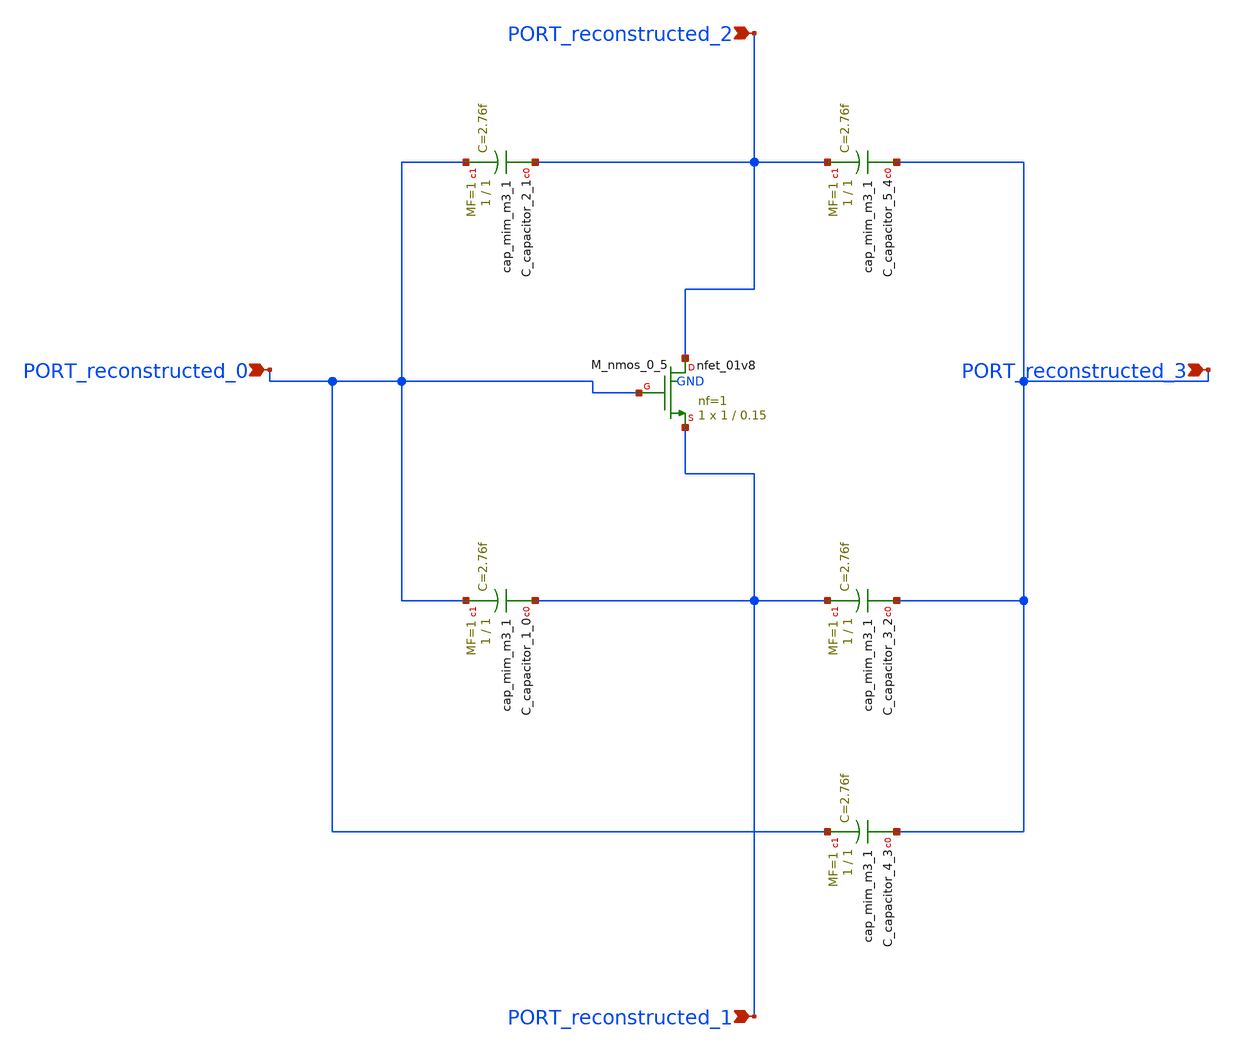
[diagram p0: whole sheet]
** sch_path: schematics/AMSNet/14.sch
**.subckt 14 PORT_reconstructed_3 PORT_reconstructed_0 PORT_reconstructed_1 PORT_reconstructed_2
*.ipin PORT_reconstructed_3
*.ipin PORT_reconstructed_0
*.ipin PORT_reconstructed_1
*.ipin PORT_reconstructed_2
XC_capacitor_1_0 PORT_reconstructed_1 PORT_reconstructed_0 sky130_fd_pr__cap_mim_m3_1 W=1 L=1 MF=1
+ m=1
XC_capacitor_2_1 PORT_reconstructed_2 PORT_reconstructed_0 sky130_fd_pr__cap_mim_m3_1 W=1 L=1 MF=1
+ m=1
XC_capacitor_3_2 PORT_reconstructed_3 PORT_reconstructed_1 sky130_fd_pr__cap_mim_m3_1 W=1 L=1 MF=1
+ m=1
XC_capacitor_4_3 PORT_reconstructed_3 PORT_reconstructed_0 sky130_fd_pr__cap_mim_m3_1 W=1 L=1 MF=1
+ m=1
XC_capacitor_5_4 PORT_reconstructed_3 PORT_reconstructed_2 sky130_fd_pr__cap_mim_m3_1 W=1 L=1 MF=1
+ m=1
XM_nmos_0_5 PORT_reconstructed_2 PORT_reconstructed_0 PORT_reconstructed_1 GND sky130_fd_pr__nfet_01v8
+ L=0.15 W=1 nf=1 ad='int((1 + 1)/2) * 1 / 1 * 0.29' as='int((1 + 2)/2) * 1 / 1 * 0.29' pd='2*int((1 + 1)/2) * (1 / 1 + 0.29)'
+ ps='2*int((1 + 2)/2) * (1 / 1 + 0.29)' nrd='0.29 / 1 ' nrs='0.29 / 1 ' sa=0 sb=0 sd=0 mult=1 m=1
**.ends
.end
